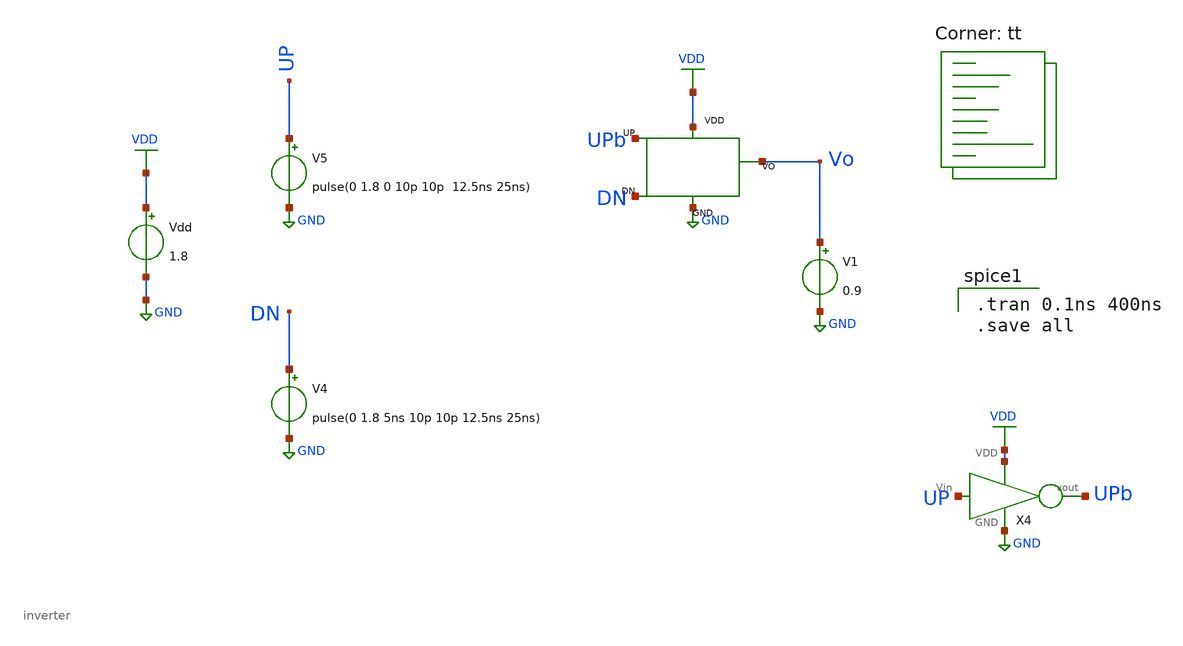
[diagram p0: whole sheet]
** sch_path: pll/pfd_cp_lf_lib/CP_tb/xschem/CP_tb.sch
**.subckt CP_tb
X1 DN UPb Vo GND VDD CP
V1 Vo GND 0.9
V4 DN GND pulse(0 1.8 5ns 10p 10p 12.5ns 25ns)
V5 UP GND pulse(0 1.8 0 10p 10p 12.5ns 25ns)
Vdd VDD GND 1.8
X4 UP UPb VDD GND inverter
**** begin user architecture code
.lib $::SKYWATER_MODELS/sky130.lib.spice tt

.tran 0.1ns 400ns
.save all


** opencircuitdesign pdks install
.lib $::SKYWATER_MODELS/sky130.lib.spice tt


**** end user architecture code
**.ends
.GLOBAL GND
.GLOBAL VDD
.end
